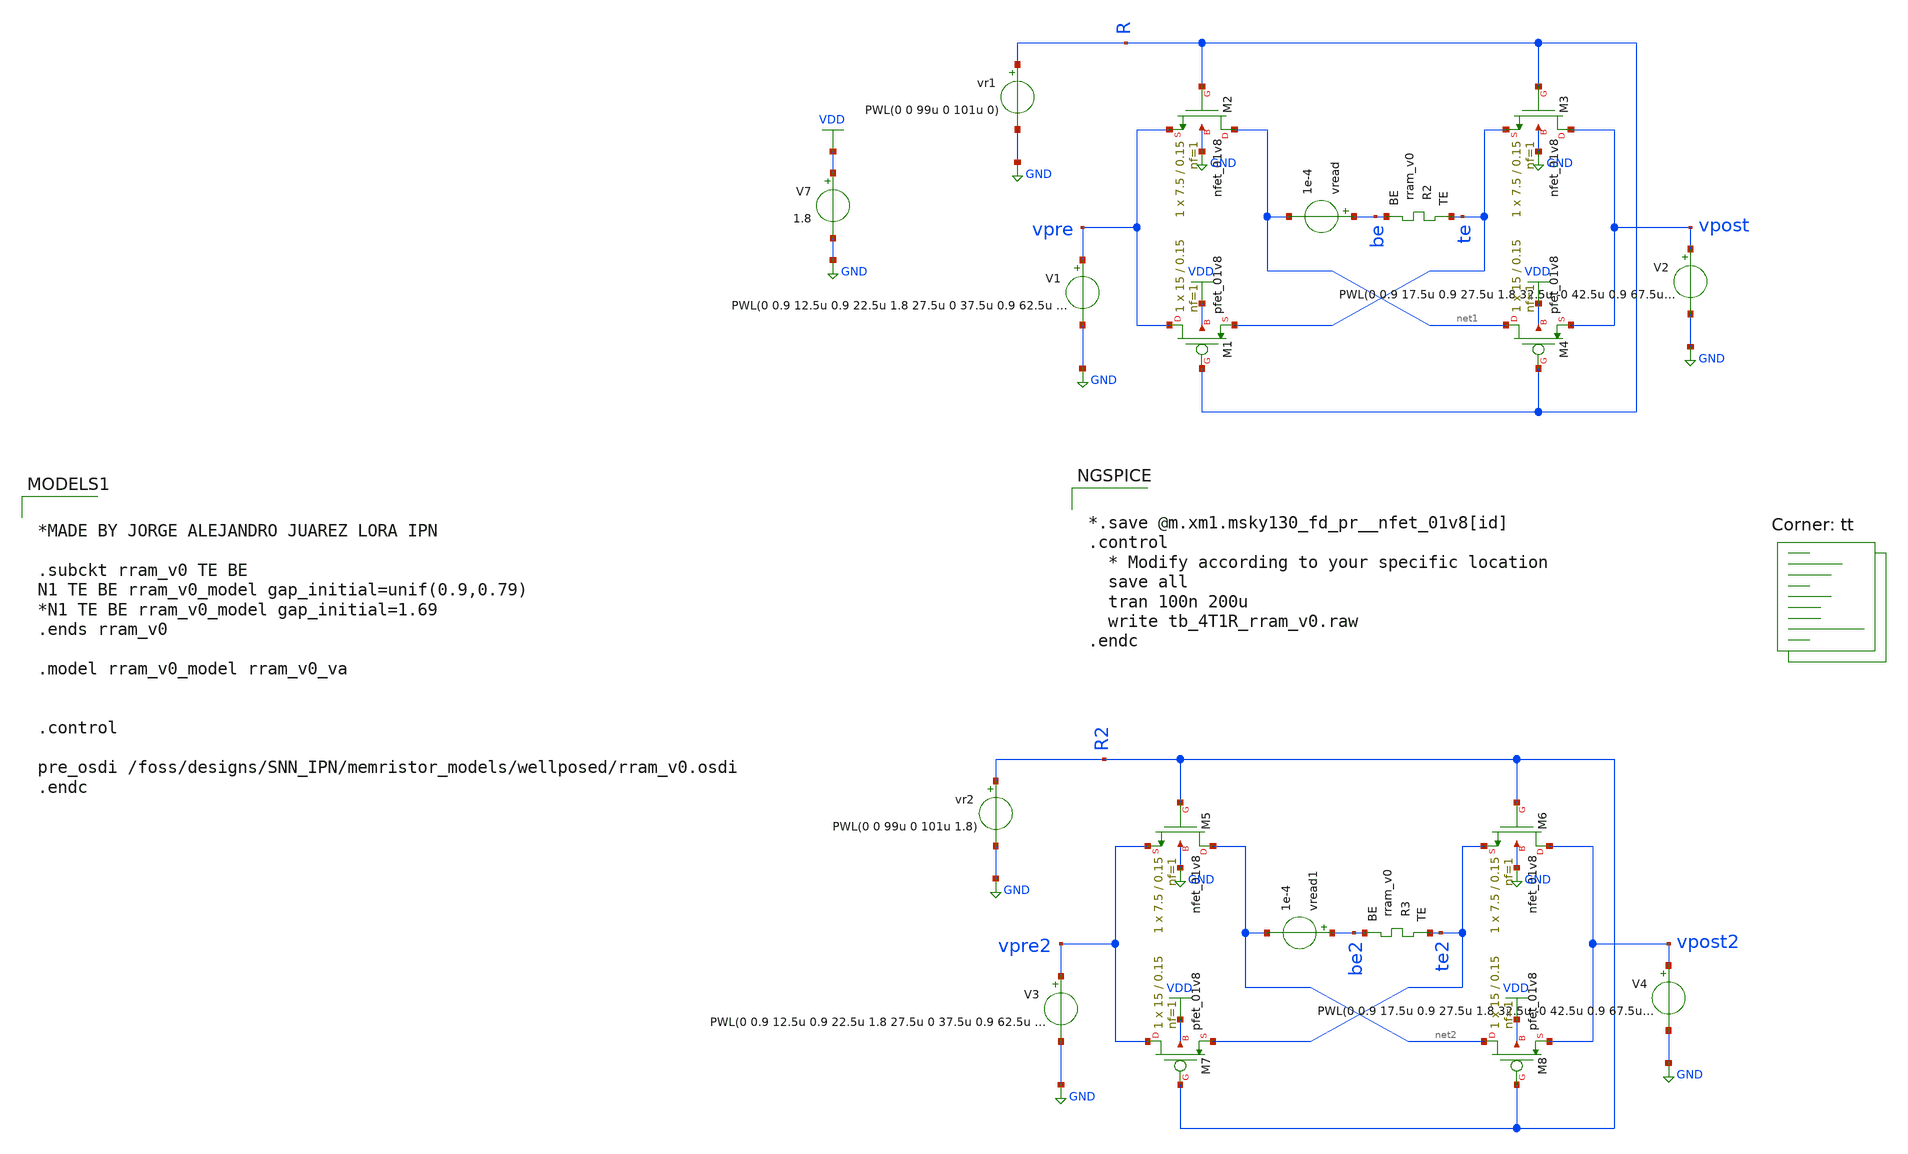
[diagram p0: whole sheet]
** sch_path: Synapse/tb_4T1R_rram_v0.sch
**.subckt tb_4T1R_rram_v0
XR2 te be rram_v0
XM2 net1 R vpre GND sky130_fd_pr__nfet_01v8 L=0.15 W=7.5 nf=1 ad='int((nf+1)/2) * W/nf * 0.29' as='int((nf+2)/2) * W/nf * 0.29'
+ pd='2*int((nf+1)/2) * (W/nf + 0.29)' ps='2*int((nf+2)/2) * (W/nf + 0.29)' nrd='0.29 / W' nrs='0.29 / W'
+ sa=0 sb=0 sd=0 mult=1 m=1
XM3 vpost R te GND sky130_fd_pr__nfet_01v8 L=0.15 W=7.5 nf=1 ad='int((nf+1)/2) * W/nf * 0.29' as='int((nf+2)/2) * W/nf * 0.29'
+ pd='2*int((nf+1)/2) * (W/nf + 0.29)' ps='2*int((nf+2)/2) * (W/nf + 0.29)' nrd='0.29 / W' nrs='0.29 / W'
+ sa=0 sb=0 sd=0 mult=1 m=1
V1 vpre GND PWL(0 0.9 12.5u 0.9 22.5u 1.8 27.5u 0 37.5u 0.9 62.5u 0.9 72.5u 1.8 77.5u 0 87.5u 0.9
+ 100u 0.9 112.5u 0.9 122.5u 1.8 127.5u 0 137.5u 0.9 162.5u 0.9 172.5u 1.8 177.5u 0 187.5u 0.9)
V2 vpost GND PWL(0 0.9 17.5u 0.9 27.5u 1.8 32.5u -0 42.5u 0.9 67.5u 0.9 77.5u 1.8 82.5u 0 92.5u 0.9
+ 100u 0.9 117.5u 0.9 127.5u 1.8 132.5u -0 142.5u 0.9 167.5u 0.9 177.5u 1.8 182.5u 0 192.5u 0.9)
vread be net1 1e-4
vr1 R GND PWL(0 0 99u 0 101u 0)
XM1 vpre R te VDD sky130_fd_pr__pfet_01v8 L=0.15 W=15 nf=1 ad='int((nf+1)/2) * W/nf * 0.29' as='int((nf+2)/2) * W/nf * 0.29'
+ pd='2*int((nf+1)/2) * (W/nf + 0.29)' ps='2*int((nf+2)/2) * (W/nf + 0.29)' nrd='0.29 / W' nrs='0.29 / W'
+ sa=0 sb=0 sd=0 mult=1 m=1
XM4 net1 R vpost VDD sky130_fd_pr__pfet_01v8 L=0.15 W=15 nf=1 ad='int((nf+1)/2) * W/nf * 0.29' as='int((nf+2)/2) * W/nf * 0.29'
+ pd='2*int((nf+1)/2) * (W/nf + 0.29)' ps='2*int((nf+2)/2) * (W/nf + 0.29)' nrd='0.29 / W' nrs='0.29 / W'
+ sa=0 sb=0 sd=0 mult=1 m=1
V7 VDD GND 1.8
XM5 net2 R2 vpre2 GND sky130_fd_pr__nfet_01v8 L=0.15 W=7.5 nf=1 ad='int((nf+1)/2) * W/nf * 0.29' as='int((nf+2)/2) * W/nf * 0.29'
+ pd='2*int((nf+1)/2) * (W/nf + 0.29)' ps='2*int((nf+2)/2) * (W/nf + 0.29)' nrd='0.29 / W' nrs='0.29 / W'
+ sa=0 sb=0 sd=0 mult=1 m=1
XM6 vpost2 R2 te2 GND sky130_fd_pr__nfet_01v8 L=0.15 W=7.5 nf=1 ad='int((nf+1)/2) * W/nf * 0.29' as='int((nf+2)/2) * W/nf * 0.29'
+ pd='2*int((nf+1)/2) * (W/nf + 0.29)' ps='2*int((nf+2)/2) * (W/nf + 0.29)' nrd='0.29 / W' nrs='0.29 / W'
+ sa=0 sb=0 sd=0 mult=1 m=1
V3 vpre2 GND PWL(0 0.9 12.5u 0.9 22.5u 1.8 27.5u 0 37.5u 0.9 62.5u 0.9 72.5u 1.8 77.5u 0 87.5u 0.9
+ 100u 0.9 112.5u 0.9 122.5u 1.8 127.5u 0 137.5u 0.9 162.5u 0.9 172.5u 1.8 177.5u 0 187.5u 0.9)
V4 vpost2 GND PWL(0 0.9 17.5u 0.9 27.5u 1.8 32.5u -0 42.5u 0.9 67.5u 0.9 77.5u 1.8 82.5u 0 92.5u 0.9
+ 100u 0.9 117.5u 0.9 127.5u 1.8 132.5u -0 142.5u 0.9 167.5u 0.9 177.5u 1.8 182.5u 0 192.5u 0.9)
vread1 be2 net2 1e-4
vr2 R2 GND PWL(0 0 99u 0 101u 1.8)
XM7 vpre2 R2 te2 VDD sky130_fd_pr__pfet_01v8 L=0.15 W=15 nf=1 ad='int((nf+1)/2) * W/nf * 0.29' as='int((nf+2)/2) * W/nf * 0.29'
+ pd='2*int((nf+1)/2) * (W/nf + 0.29)' ps='2*int((nf+2)/2) * (W/nf + 0.29)' nrd='0.29 / W' nrs='0.29 / W'
+ sa=0 sb=0 sd=0 mult=1 m=1
XM8 net2 R2 vpost2 VDD sky130_fd_pr__pfet_01v8 L=0.15 W=15 nf=1 ad='int((nf+1)/2) * W/nf * 0.29' as='int((nf+2)/2) * W/nf * 0.29'
+ pd='2*int((nf+1)/2) * (W/nf + 0.29)' ps='2*int((nf+2)/2) * (W/nf + 0.29)' nrd='0.29 / W' nrs='0.29 / W'
+ sa=0 sb=0 sd=0 mult=1 m=1
XR3 te2 be2 rram_v0
**** begin user architecture code


*.save @m.xm1.msky130_fd_pr__nfet_01v8[id]
.control
  * Modify according to your specific location
  save all
  tran 100n 200u
  write tb_4T1R_rram_v0.raw
.endc



.lib $::SKYWATER_MODELS/sky130.lib.spice tt

*MADE BY JORGE ALEJANDRO JUAREZ LORA IPN

.subckt rram_v0 TE BE
N1 TE BE rram_v0_model gap_initial=unif(0.9,0.79)
*N1 TE BE rram_v0_model gap_initial=1.69
.ends rram_v0

.model rram_v0_model rram_v0_va


.control

pre_osdi /foss/designs/SNN_IPN/memristor_models/wellposed/rram_v0.osdi
.endc


**** end user architecture code
**.ends
.GLOBAL GND
.GLOBAL VDD
.end
